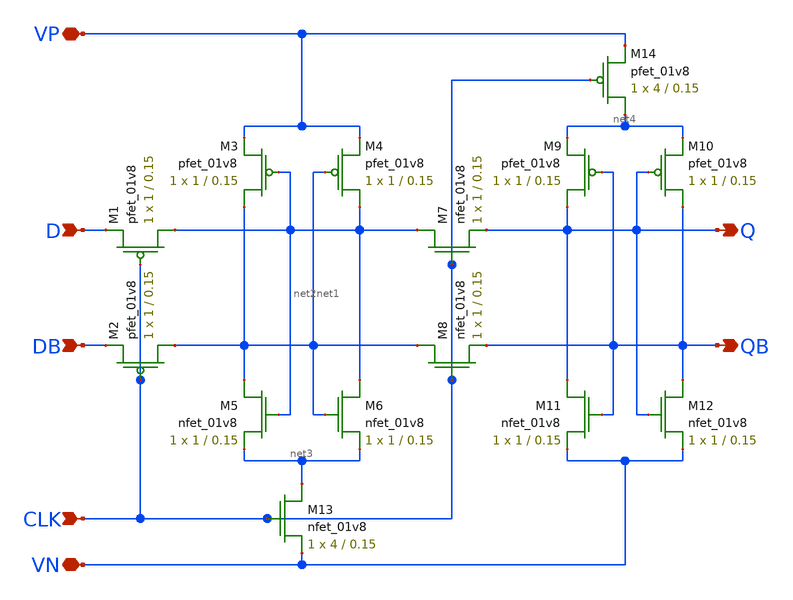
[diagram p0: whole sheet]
** sch_path: MP2/xschem/final/csrl_dff3.sch
**.subckt csrl_dff3 D DB CLK Q QB VP VN
*.ipin D
*.ipin DB
*.ipin CLK
*.opin Q
*.opin QB
*.iopin VP
*.iopin VN
XM1 net2 CLK D VDD sky130_fd_pr__pfet_01v8 L=0.15 W=1 nf=1 ad='int((nf+1)/2) * W/nf * 0.29' as='int((nf+2)/2) * W/nf * 0.29'
+ pd='2*int((nf+1)/2) * (W/nf + 0.29)' ps='2*int((nf+2)/2) * (W/nf + 0.29)' nrd='0.29 / W' nrs='0.29 / W'
+ sa=0 sb=0 sd=0 mult=1 m=1
XM2 net1 CLK DB VDD sky130_fd_pr__pfet_01v8 L=0.15 W=1 nf=1 ad='int((nf+1)/2) * W/nf * 0.29' as='int((nf+2)/2) * W/nf * 0.29'
+ pd='2*int((nf+1)/2) * (W/nf + 0.29)' ps='2*int((nf+2)/2) * (W/nf + 0.29)' nrd='0.29 / W' nrs='0.29 / W'
+ sa=0 sb=0 sd=0 mult=1 m=1
XM3 net1 net2 VP VDD sky130_fd_pr__pfet_01v8 L=0.15 W=1 nf=1 ad='int((nf+1)/2) * W/nf * 0.29' as='int((nf+2)/2) * W/nf * 0.29'
+ pd='2*int((nf+1)/2) * (W/nf + 0.29)' ps='2*int((nf+2)/2) * (W/nf + 0.29)' nrd='0.29 / W' nrs='0.29 / W'
+ sa=0 sb=0 sd=0 mult=1 m=1
XM4 net2 net1 VP VDD sky130_fd_pr__pfet_01v8 L=0.15 W=1 nf=1 ad='int((nf+1)/2) * W/nf * 0.29' as='int((nf+2)/2) * W/nf * 0.29'
+ pd='2*int((nf+1)/2) * (W/nf + 0.29)' ps='2*int((nf+2)/2) * (W/nf + 0.29)' nrd='0.29 / W' nrs='0.29 / W'
+ sa=0 sb=0 sd=0 mult=1 m=1
XM5 net1 net2 net3 GND sky130_fd_pr__nfet_01v8 L=0.15 W=1 nf=1 ad='int((nf+1)/2) * W/nf * 0.29' as='int((nf+2)/2) * W/nf * 0.29'
+ pd='2*int((nf+1)/2) * (W/nf + 0.29)' ps='2*int((nf+2)/2) * (W/nf + 0.29)' nrd='0.29 / W' nrs='0.29 / W'
+ sa=0 sb=0 sd=0 mult=1 m=1
XM6 net2 net1 net3 GND sky130_fd_pr__nfet_01v8 L=0.15 W=1 nf=1 ad='int((nf+1)/2) * W/nf * 0.29' as='int((nf+2)/2) * W/nf * 0.29'
+ pd='2*int((nf+1)/2) * (W/nf + 0.29)' ps='2*int((nf+2)/2) * (W/nf + 0.29)' nrd='0.29 / W' nrs='0.29 / W'
+ sa=0 sb=0 sd=0 mult=1 m=1
XM7 net2 CLK Q GND sky130_fd_pr__nfet_01v8 L=0.15 W=1 nf=1 ad='int((nf+1)/2) * W/nf * 0.29' as='int((nf+2)/2) * W/nf * 0.29'
+ pd='2*int((nf+1)/2) * (W/nf + 0.29)' ps='2*int((nf+2)/2) * (W/nf + 0.29)' nrd='0.29 / W' nrs='0.29 / W'
+ sa=0 sb=0 sd=0 mult=1 m=1
XM8 net1 CLK QB GND sky130_fd_pr__nfet_01v8 L=0.15 W=1 nf=1 ad='int((nf+1)/2) * W/nf * 0.29' as='int((nf+2)/2) * W/nf * 0.29'
+ pd='2*int((nf+1)/2) * (W/nf + 0.29)' ps='2*int((nf+2)/2) * (W/nf + 0.29)' nrd='0.29 / W' nrs='0.29 / W'
+ sa=0 sb=0 sd=0 mult=1 m=1
XM9 Q QB net4 VDD sky130_fd_pr__pfet_01v8 L=0.15 W=1 nf=1 ad='int((nf+1)/2) * W/nf * 0.29' as='int((nf+2)/2) * W/nf * 0.29'
+ pd='2*int((nf+1)/2) * (W/nf + 0.29)' ps='2*int((nf+2)/2) * (W/nf + 0.29)' nrd='0.29 / W' nrs='0.29 / W'
+ sa=0 sb=0 sd=0 mult=1 m=1
XM10 QB Q net4 VDD sky130_fd_pr__pfet_01v8 L=0.15 W=1 nf=1 ad='int((nf+1)/2) * W/nf * 0.29' as='int((nf+2)/2) * W/nf * 0.29'
+ pd='2*int((nf+1)/2) * (W/nf + 0.29)' ps='2*int((nf+2)/2) * (W/nf + 0.29)' nrd='0.29 / W' nrs='0.29 / W'
+ sa=0 sb=0 sd=0 mult=1 m=1
XM11 Q QB VN GND sky130_fd_pr__nfet_01v8 L=0.15 W=1 nf=1 ad='int((nf+1)/2) * W/nf * 0.29' as='int((nf+2)/2) * W/nf * 0.29'
+ pd='2*int((nf+1)/2) * (W/nf + 0.29)' ps='2*int((nf+2)/2) * (W/nf + 0.29)' nrd='0.29 / W' nrs='0.29 / W'
+ sa=0 sb=0 sd=0 mult=1 m=1
XM12 QB Q VN GND sky130_fd_pr__nfet_01v8 L=0.15 W=1 nf=1 ad='int((nf+1)/2) * W/nf * 0.29' as='int((nf+2)/2) * W/nf * 0.29'
+ pd='2*int((nf+1)/2) * (W/nf + 0.29)' ps='2*int((nf+2)/2) * (W/nf + 0.29)' nrd='0.29 / W' nrs='0.29 / W'
+ sa=0 sb=0 sd=0 mult=1 m=1
XM13 net3 CLK VN GND sky130_fd_pr__nfet_01v8 L=0.15 W=4 nf=1 ad='int((nf+1)/2) * W/nf * 0.29' as='int((nf+2)/2) * W/nf * 0.29'
+ pd='2*int((nf+1)/2) * (W/nf + 0.29)' ps='2*int((nf+2)/2) * (W/nf + 0.29)' nrd='0.29 / W' nrs='0.29 / W'
+ sa=0 sb=0 sd=0 mult=1 m=1
XM14 net4 CLK VP VDD sky130_fd_pr__pfet_01v8 L=0.15 W=4 nf=1 ad='int((nf+1)/2) * W/nf * 0.29' as='int((nf+2)/2) * W/nf * 0.29'
+ pd='2*int((nf+1)/2) * (W/nf + 0.29)' ps='2*int((nf+2)/2) * (W/nf + 0.29)' nrd='0.29 / W' nrs='0.29 / W'
+ sa=0 sb=0 sd=0 mult=1 m=1
**.ends
.end
